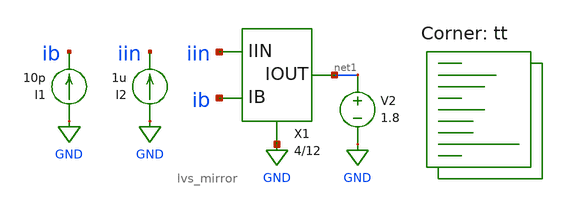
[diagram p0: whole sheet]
** sch_path: dac/schematic/lvs_mirror_tb.sch
**.subckt lvs_mirror_tb
I1 GND ib 10p
I2 GND iin 1u
V2 net1 GND 1.8
X1 GND iin ib net1 lvs_mirror u_w=4 u_l=12 m=2 r=1M
**** begin user architecture code
.lib $::SKYWATER_MODELS/sky130.lib.spice tt

.control
  set wr_vecnames
  set wr_singlescale
  dc V2 0 1.8 0.01
  wrdata ~/documents/git/madvlsi/dac/build/lvs_mirror/lvs_mirror_tb.txt i(V2)
.endc

**** end user architecture code
**.ends
.GLOBAL GND
.end
